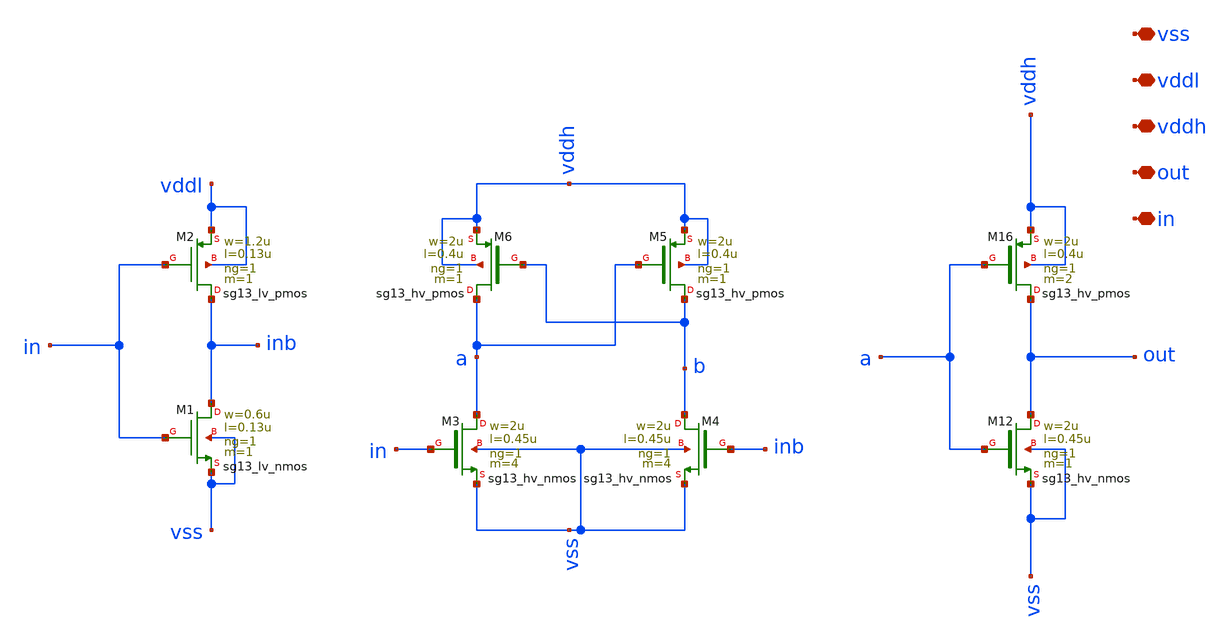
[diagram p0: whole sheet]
** sch_path: circuit_files/sar_adc_test/xschem/level_shifter_1v2_to_3v3.sch
**.subckt level_shifter_1v2_to_3v3 vddl vddh out vss in
*.iopin vddl
*.iopin vddh
*.iopin out
*.iopin vss
*.iopin in
XM1 inb in vss vss sg13_lv_nmos w=0.6u l=0.13u ng=1 m=1 mm_ok=1
XM2 inb in vddl vddl sg13_lv_pmos w=1.2u l=0.13u ng=1 m=1 mm_ok=1
XM3 a in vss vss sg13_hv_nmos w=2u l=0.45u ng=1 m=4 mm_ok=1
XM4 b inb vss vss sg13_hv_nmos w=2u l=0.45u ng=1 m=4 mm_ok=1
XM5 b a vddh vddh sg13_hv_pmos w=2u l=0.4u ng=1 m=1 mm_ok=1
XM6 a b vddh vddh sg13_hv_pmos w=2u l=0.4u ng=1 m=1 mm_ok=1
XM12 out a vss vss sg13_hv_nmos w=2u l=0.45u ng=1 m=1 mm_ok=1
XM16 out a vddh vddh sg13_hv_pmos w=2u l=0.4u ng=1 m=2 mm_ok=1
**.ends
.end
